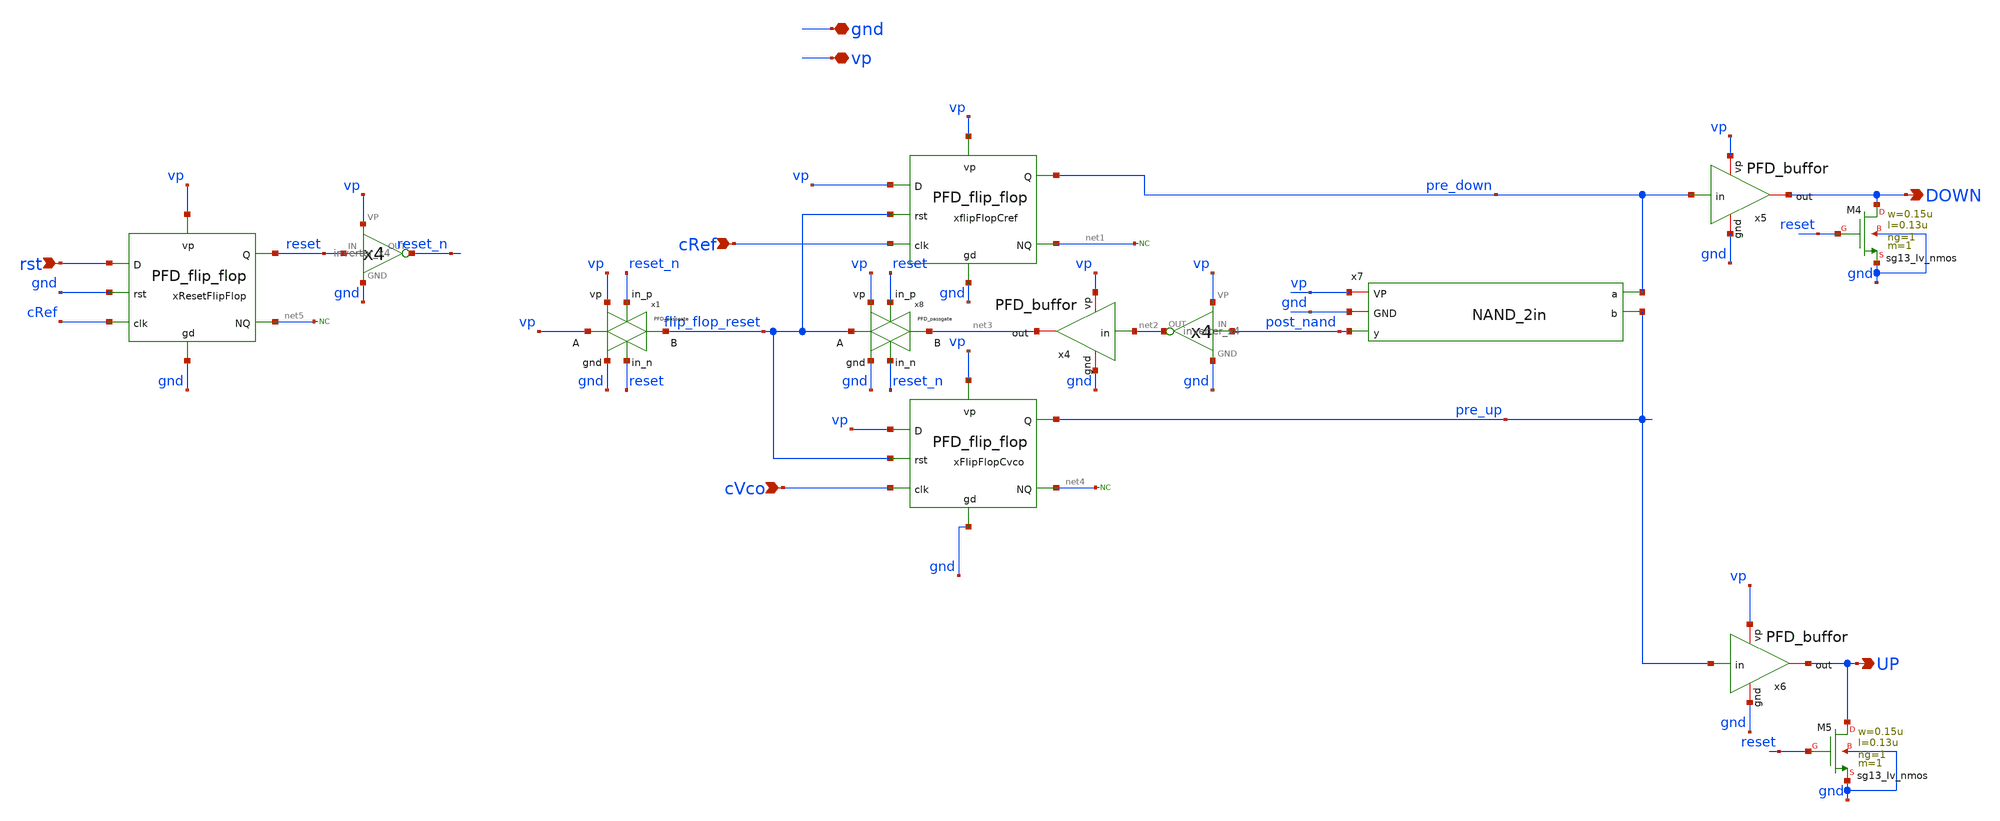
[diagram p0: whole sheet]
** sch_path: schematics/PFD/PFD_cell_2.sch
**.subckt PFD_cell_2 gnd vp cRef cVco rst UP DOWN
*.iopin gnd
*.iopin vp
*.ipin cRef
*.ipin cVco
*.ipin rst
*.opin UP
*.opin DOWN
x4 gnd vp net3 net2 PFD_buffor
x5 gnd vp DOWN pre_down PFD_buffor
x6 gnd vp UP pre_up PFD_buffor
x7 vp gnd pre_down post_nand pre_up NAND_2in
* noconn #net1
* noconn #net4
x9 reset reset_n vp gnd inverter_x4
xflipFlopCref cRef flip_flop_reset vp pre_down net1 vp gnd PFD_flip_flop
xFlipFlopCvco cVco flip_flop_reset vp pre_up net4 vp gnd PFD_flip_flop
x1 reset vp vp flip_flop_reset gnd reset_n PFD_passgate
x11 post_nand net2 vp gnd inverter_x4
XM4 DOWN reset gnd gnd sg13_lv_nmos w=0.15u l=0.13u ng=1 m=1 mm_ok=1
XM5 UP reset gnd gnd sg13_lv_nmos w=0.15u l=0.13u ng=1 m=1 mm_ok=1
x8 reset_n vp flip_flop_reset net3 gnd reset PFD_passgate
* noconn #net5
xResetFlipFlop cRef gnd rst reset net5 vp gnd PFD_flip_flop
**.ends
.end
